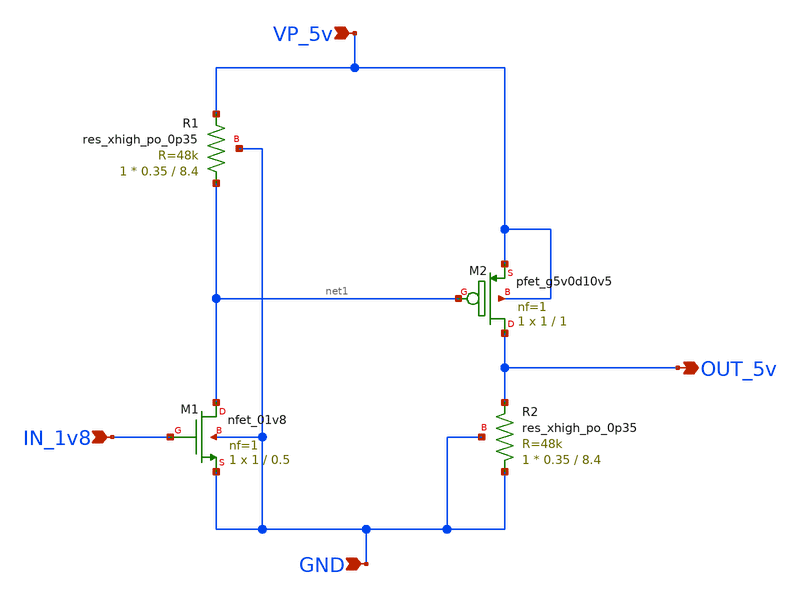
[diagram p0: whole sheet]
** sch_path: ADC/16bit_C2C/MagicAndSpice/EE431_FinalProj/Shift_1v8_to_5v.sch
**.subckt Shift_1v8_to_5v IN_1v8 VP_5v GND OUT_5v
*.ipin IN_1v8
*.ipin VP_5v
*.ipin GND
*.opin OUT_5v
XR1 net1 VP_5v GND sky130_fd_pr__res_xhigh_po_0p35 L=8.4 mult=1 m=1
XR2 GND OUT_5v GND sky130_fd_pr__res_xhigh_po_0p35 L=8.4 mult=1 m=1
XM1 net1 IN_1v8 GND GND sky130_fd_pr__nfet_01v8 L=0.5 W=1 nf=1 ad='int((nf+1)/2) * W/nf * 0.29' as='int((nf+2)/2) * W/nf * 0.29'
+ pd='2*int((nf+1)/2) * (W/nf + 0.29)' ps='2*int((nf+2)/2) * (W/nf + 0.29)' nrd='0.29 / W' nrs='0.29 / W'
+ sa=0 sb=0 sd=0 mult=1 m=1
XM2 OUT_5v net1 VP_5v VP_5v sky130_fd_pr__pfet_g5v0d10v5 L=1 W=1 nf=1 ad='int((nf+1)/2) * W/nf * 0.29'
+ as='int((nf+2)/2) * W/nf * 0.29' pd='2*int((nf+1)/2) * (W/nf + 0.29)' ps='2*int((nf+2)/2) * (W/nf + 0.29)'
+ nrd='0.29 / W' nrs='0.29 / W' sa=0 sb=0 sd=0 mult=1 m=1
**.ends
.end
